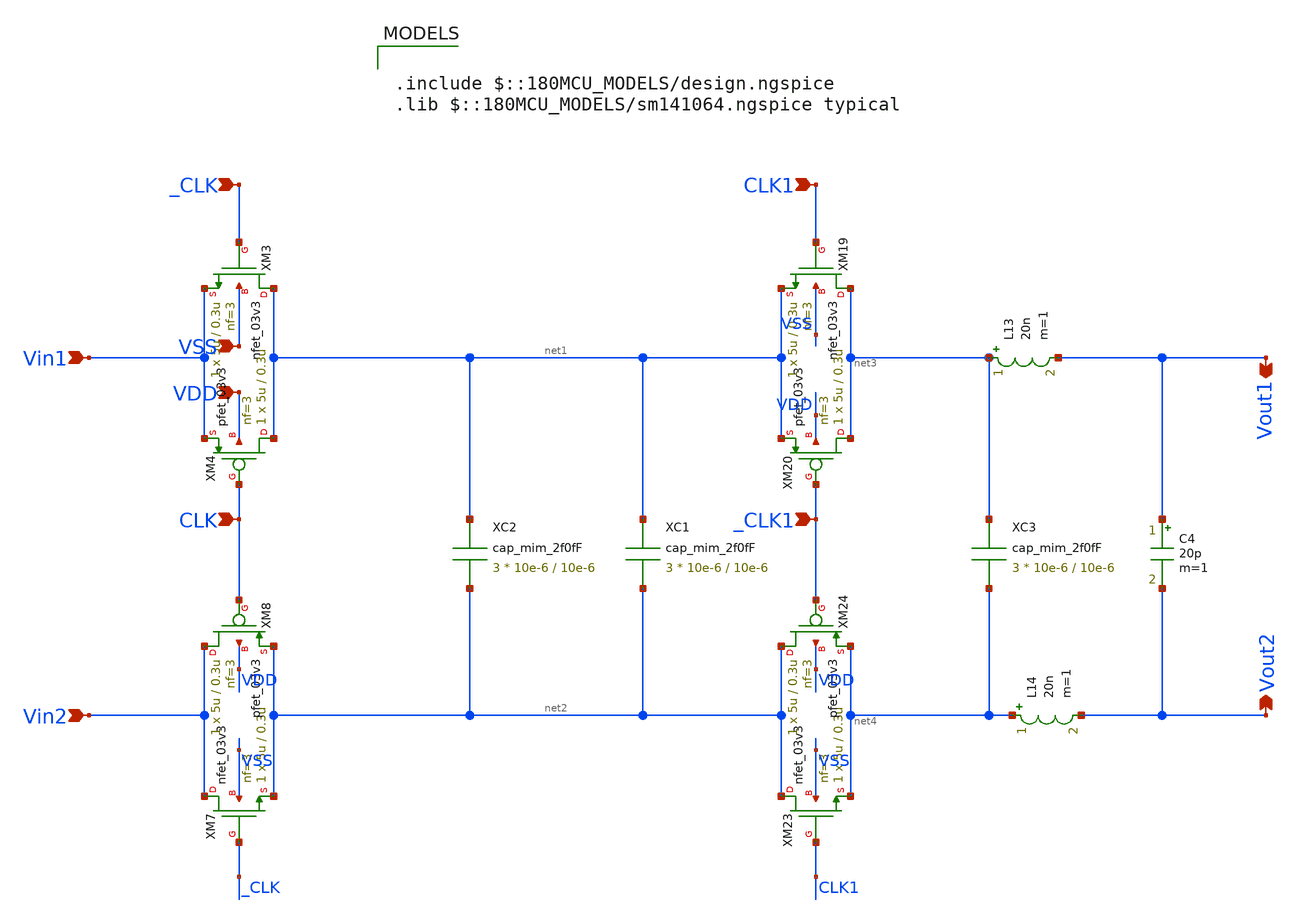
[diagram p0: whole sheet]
** sch_path: ISSCC26/submitted_notebooks/Low Mismatch 4 Channels Instrumentation Amplifier EEG/Switched-Cap Low Pass Filter/Schematic and Testbench/lpf.sch
**.subckt lpf VSS VDD _CLK CLK Vin1 Vin2 CLK1 _CLK1 Vout1 Vout2
*.ipin VSS
*.ipin VDD
*.ipin _CLK
*.ipin CLK
*.ipin Vin1
*.ipin Vin2
*.ipin CLK1
*.ipin _CLK1
*.opin Vout1
*.opin Vout2
XM3 net1 _CLK Vin1 VSS nfet_03v3 L=0.3u W=5u nf=3 ad='int((nf+1)/2) * W/nf * 0.18u' as='int((nf+2)/2) * W/nf * 0.18u'
+ pd='2*int((nf+1)/2) * (W/nf + 0.18u)' ps='2*int((nf+2)/2) * (W/nf + 0.18u)' nrd='0.18u / W' nrs='0.18u / W'
+ sa=0 sb=0 sd=0 m=1
XM4 net1 CLK Vin1 VDD pfet_03v3 L=0.3u W=5u nf=3 ad='int((nf+1)/2) * W/nf * 0.18u' as='int((nf+2)/2) * W/nf * 0.18u'
+ pd='2*int((nf+1)/2) * (W/nf + 0.18u)' ps='2*int((nf+2)/2) * (W/nf + 0.18u)' nrd='0.18u / W' nrs='0.18u / W'
+ sa=0 sb=0 sd=0 m=1
XM7 Vin2 _CLK net2 VSS nfet_03v3 L=0.3u W=5u nf=3 ad='int((nf+1)/2) * W/nf * 0.18u' as='int((nf+2)/2) * W/nf * 0.18u'
+ pd='2*int((nf+1)/2) * (W/nf + 0.18u)' ps='2*int((nf+2)/2) * (W/nf + 0.18u)' nrd='0.18u / W' nrs='0.18u / W'
+ sa=0 sb=0 sd=0 m=1
XM8 Vin2 CLK net2 VDD pfet_03v3 L=0.3u W=5u nf=3 ad='int((nf+1)/2) * W/nf * 0.18u' as='int((nf+2)/2) * W/nf * 0.18u'
+ pd='2*int((nf+1)/2) * (W/nf + 0.18u)' ps='2*int((nf+2)/2) * (W/nf + 0.18u)' nrd='0.18u / W' nrs='0.18u / W'
+ sa=0 sb=0 sd=0 m=1
XM19 net3 CLK1 net1 VSS nfet_03v3 L=0.3u W=5u nf=3 ad='int((nf+1)/2) * W/nf * 0.18u' as='int((nf+2)/2) * W/nf * 0.18u'
+ pd='2*int((nf+1)/2) * (W/nf + 0.18u)' ps='2*int((nf+2)/2) * (W/nf + 0.18u)' nrd='0.18u / W' nrs='0.18u / W'
+ sa=0 sb=0 sd=0 m=1
XM20 net3 _CLK1 net1 VDD pfet_03v3 L=0.3u W=5u nf=3 ad='int((nf+1)/2) * W/nf * 0.18u' as='int((nf+2)/2) * W/nf * 0.18u'
+ pd='2*int((nf+1)/2) * (W/nf + 0.18u)' ps='2*int((nf+2)/2) * (W/nf + 0.18u)' nrd='0.18u / W' nrs='0.18u / W'
+ sa=0 sb=0 sd=0 m=1
XM23 net2 CLK1 net4 VSS nfet_03v3 L=0.3u W=5u nf=3 ad='int((nf+1)/2) * W/nf * 0.18u' as='int((nf+2)/2) * W/nf * 0.18u'
+ pd='2*int((nf+1)/2) * (W/nf + 0.18u)' ps='2*int((nf+2)/2) * (W/nf + 0.18u)' nrd='0.18u / W' nrs='0.18u / W'
+ sa=0 sb=0 sd=0 m=1
XM24 net2 _CLK1 net4 VDD pfet_03v3 L=0.3u W=5u nf=3 ad='int((nf+1)/2) * W/nf * 0.18u' as='int((nf+2)/2) * W/nf * 0.18u'
+ pd='2*int((nf+1)/2) * (W/nf + 0.18u)' ps='2*int((nf+2)/2) * (W/nf + 0.18u)' nrd='0.18u / W' nrs='0.18u / W'
+ sa=0 sb=0 sd=0 m=1
XC1 net1 net2 cap_mim_2f0fF c_width=10e-6 c_length=10e-6 m=3
XC2 net1 net2 cap_mim_2f0fF c_width=10e-6 c_length=10e-6 m=3
XC3 net3 net4 cap_mim_2f0fF c_width=10e-6 c_length=10e-6 m=3
L13 net3 Vout1 20n m=1
C4 Vout1 Vout2 20p m=1
L14 net4 Vout2 20n m=1
**** begin user architecture code

.include $::180MCU_MODELS/design.ngspice
.lib $::180MCU_MODELS/sm141064.ngspice typical

**** end user architecture code
**.ends
.end
